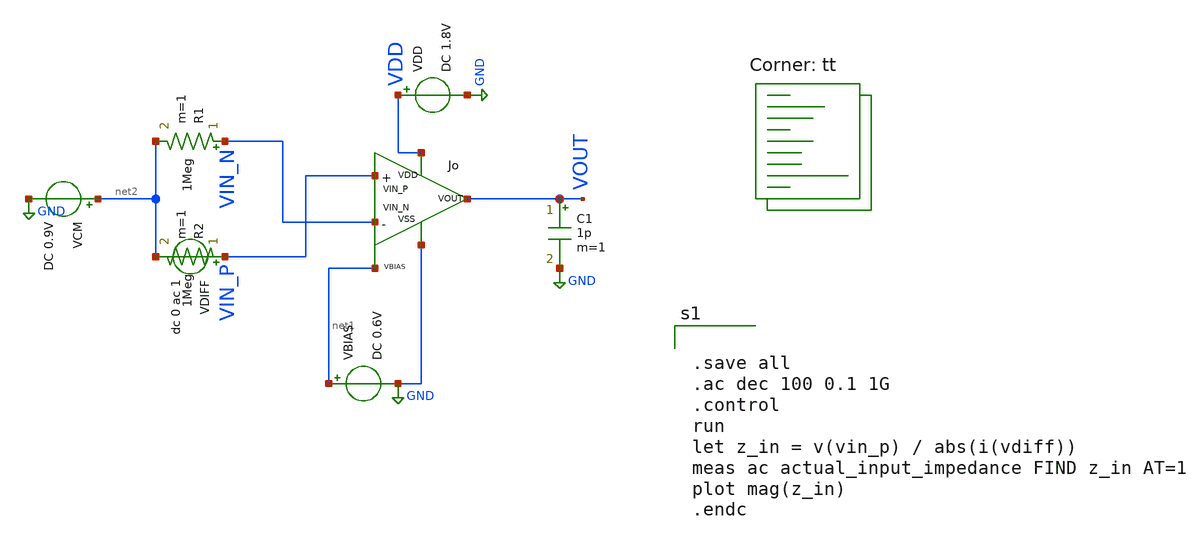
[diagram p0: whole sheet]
** sch_path: analog/bootcamp_opamp/build/schematic/input_tb_impedance.sch
**.subckt input_tb_impedance
x1 VOUT VIN_P VIN_N VDD GND net1 myopamp
VCM net2 GND DC 0.9V
VDD VDD GND DC 1.8V
VBIAS net1 GND DC 0.6V
C1 VOUT GND 1p m=1
VDIFF VIN_P net2 dc 0 ac 1
.save i(vdiff)
R1 VIN_N net2 1Meg m=1
R2 VIN_P net2 1Meg m=1
**** begin user architecture code


.save all
.ac dec 100 0.1 1G
.control
run
let z_in = v(vin_p) / abs(i(vdiff))
meas ac actual_input_impedance FIND z_in AT=1
plot mag(z_in)
.endc


.lib $::SKYWATER_MODELS/sky130.lib.spice tt
**** end user architecture code
**.ends

* expanding   symbol:  myopamp.sym # of pins=6
** sym_path: analog/bootcamp_opamp/build/schematic/myopamp.sym
** sch_path: analog/bootcamp_opamp/build/schematic/myopamp.sch
.subckt myopamp VOUT VIN_P VIN_N VDD VSS VBIAS
*.ipin VIN_N
*.ipin VIN_P
*.ipin VBIAS
*.opin VOUT
*.iopin VDD
*.iopin VSS
XM1 net2 VIN_N net1 VSS sky130_fd_pr__nfet_01v8 L=0.500 W=0.420 nf=1 ad='int((nf+1)/2) * W/nf * 0.29'
+ as='int((nf+2)/2) * W/nf * 0.29' pd='2*int((nf+1)/2) * (W/nf + 0.29)' ps='2*int((nf+2)/2) * (W/nf + 0.29)'
+ nrd='0.29 / W' nrs='0.29 / W' sa=0 sb=0 sd=0 mult=1 m=1
XM2 net3 VIN_P net1 VSS sky130_fd_pr__nfet_01v8 L=0.500 W=0.420 nf=1 ad='int((nf+1)/2) * W/nf * 0.29'
+ as='int((nf+2)/2) * W/nf * 0.29' pd='2*int((nf+1)/2) * (W/nf + 0.29)' ps='2*int((nf+2)/2) * (W/nf + 0.29)'
+ nrd='0.29 / W' nrs='0.29 / W' sa=0 sb=0 sd=0 mult=1 m=1
XM3 net2 net2 VDD VDD sky130_fd_pr__pfet_01v8 L=1.000 W=0.893 nf=1 ad='int((nf+1)/2) * W/nf * 0.29' as='int((nf+2)/2) * W/nf * 0.29'
+ pd='2*int((nf+1)/2) * (W/nf + 0.29)' ps='2*int((nf+2)/2) * (W/nf + 0.29)' nrd='0.29 / W' nrs='0.29 / W'
+ sa=0 sb=0 sd=0 mult=1 m=1
XM4 net3 net2 VDD VDD sky130_fd_pr__pfet_01v8 L=1.000 W=0.893 nf=1 ad='int((nf+1)/2) * W/nf * 0.29' as='int((nf+2)/2) * W/nf * 0.29'
+ pd='2*int((nf+1)/2) * (W/nf + 0.29)' ps='2*int((nf+2)/2) * (W/nf + 0.29)' nrd='0.29 / W' nrs='0.29 / W'
+ sa=0 sb=0 sd=0 mult=1 m=1
XM5 net1 VBIAS VSS VSS sky130_fd_pr__nfet_01v8 L=1.000 W=0.463 nf=1 ad='int((nf+1)/2) * W/nf * 0.29'
+ as='int((nf+2)/2) * W/nf * 0.29' pd='2*int((nf+1)/2) * (W/nf + 0.29)' ps='2*int((nf+2)/2) * (W/nf + 0.29)'
+ nrd='0.29 / W' nrs='0.29 / W' sa=0 sb=0 sd=0 mult=1 m=1
XM6 VOUT net3 VDD VDD sky130_fd_pr__pfet_01v8 L=0.500 W=52.380 nf=1 ad='int((nf+1)/2) * W/nf * 0.29'
+ as='int((nf+2)/2) * W/nf * 0.29' pd='2*int((nf+1)/2) * (W/nf + 0.29)' ps='2*int((nf+2)/2) * (W/nf + 0.29)'
+ nrd='0.29 / W' nrs='0.29 / W' sa=0 sb=0 sd=0 mult=3 m=3
XM7 VOUT VBIAS VSS VSS sky130_fd_pr__nfet_01v8 L=1.000 W=48.290 nf=1 ad='int((nf+1)/2) * W/nf * 0.29'
+ as='int((nf+2)/2) * W/nf * 0.29' pd='2*int((nf+1)/2) * (W/nf + 0.29)' ps='2*int((nf+2)/2) * (W/nf + 0.29)'
+ nrd='0.29 / W' nrs='0.29 / W' sa=0 sb=0 sd=0 mult=3 m=3
XC1 net3 VOUT sky130_fd_pr__cap_mim_m3_1 W=10 L=12.5 MF=1 m=1
.ends

.GLOBAL GND
.end
